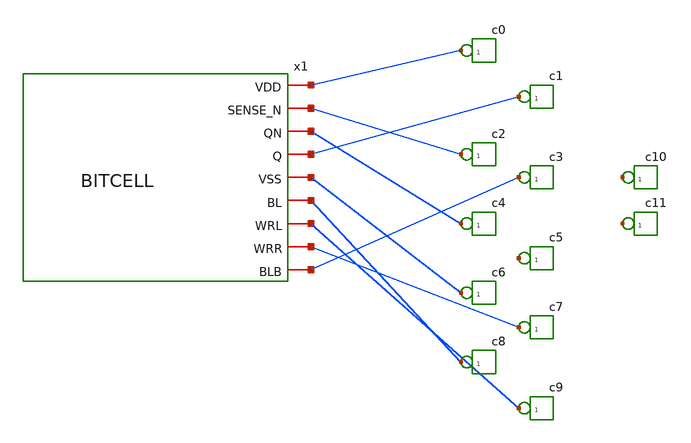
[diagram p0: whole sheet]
** sch_path: top.sch
**.subckt top
x1 net1 net2 net3 net4 net5 net6 net7 net8 net9 BITCELL
*connector(1,1) ?1 net1
*connector(1,1) ?1 net4
*connector(1,1) ?1 net2
*connector(1,1) ?1 net9
*connector(1,1) ?1 net3
*connector(1,1) ?1 net10
*connector(1,1) ?1 net5
*connector(1,1) ?1 net8
*connector(1,1) ?1 net6
*connector(1,1) ?1 net7
*connector(1,1) ?1 net11
*connector(1,1) ?1 net12
**.ends

* expanding   symbol:  /home/jackclar/mramSkywater/BITCELL.sym # of pins=9
** sym_path: BITCELL.sym
** sch_path: BITCELL.sch
.subckt BITCELL VDD SENSE_N QN Q VSS BL WRL WRR BLB
*.iopin VDD
*.iopin SENSE_N
*.iopin QN
*.iopin Q
*.iopin VSS
*.iopin BL
*.iopin WRR
*.iopin WRL
*.iopin BLB
x1 VDD SENSE_N QN Q VSS net2 net1 SENSEAMP
XR1 net1 BLB sky130_fd_pr__PMAMTJ Diameter=80E-9 t_fre=1.8E-9 t_ox=1.1E-9 T0=300 JOULE=2 IS=1
+ TMR_G=1.1 IC_G=1 RA_G=1
XR2 net2 BLB sky130_fd_pr__PMAMTJ Diameter=80E-9 t_fre=1.8E-9 t_ox=1.1E-9 T0=300 JOULE=2 IS=1
+ TMR_G=1.1 IC_G=1 RA_G=1
XM1 net1 WRL BL VSS sky130_fd_pr__nfet_01v8 L=0.15 W=1 nf=1 ad='int((nf+1)/2) * W/nf * 0.29' as='int((nf+2)/2) * W/nf * 0.29'
+ pd='2*int((nf+1)/2) * (W/nf + 0.29)' ps='2*int((nf+2)/2) * (W/nf + 0.29)' nrd='0.29 / W' nrs='0.29 / W'
+ sa=0 sb=0 sd=0 mult=1 m=1
XM2 net2 WRR BL VSS sky130_fd_pr__nfet_01v8 L=0.15 W=1 nf=1 ad='int((nf+1)/2) * W/nf * 0.29' as='int((nf+2)/2) * W/nf * 0.29'
+ pd='2*int((nf+1)/2) * (W/nf + 0.29)' ps='2*int((nf+2)/2) * (W/nf + 0.29)' nrd='0.29 / W' nrs='0.29 / W'
+ sa=0 sb=0 sd=0 mult=1 m=1
.ends


* expanding   symbol:  /home/jackclar/mramSkywater/SENSEAMP.sym # of pins=7
** sym_path: SENSEAMP.sym
** sch_path: SENSEAMP.sch
.subckt SENSEAMP VDD SENSE_N QN Q VSS I0 I1
*.iopin I1
*.iopin I0
*.iopin Q
*.iopin QN
*.iopin SENSE_N
*.iopin VDD
*.iopin VSS
XM3 Q SENSE_N VDD VDD sky130_fd_pr__pfet_01v8 L=0.15 W=1 nf=1 ad='int((nf+1)/2) * W/nf * 0.29' as='int((nf+2)/2) * W/nf * 0.29'
+ pd='2*int((nf+1)/2) * (W/nf + 0.29)' ps='2*int((nf+2)/2) * (W/nf + 0.29)' nrd='0.29 / W' nrs='0.29 / W'
+ sa=0 sb=0 sd=0 mult=1 m=1
XM1 Q QN VDD VDD sky130_fd_pr__pfet_01v8 L=0.15 W=1 nf=1 ad='int((nf+1)/2) * W/nf * 0.29' as='int((nf+2)/2) * W/nf * 0.29'
+ pd='2*int((nf+1)/2) * (W/nf + 0.29)' ps='2*int((nf+2)/2) * (W/nf + 0.29)' nrd='0.29 / W' nrs='0.29 / W'
+ sa=0 sb=0 sd=0 mult=1 m=1
XM2 QN Q VDD VDD sky130_fd_pr__pfet_01v8 L=0.15 W=1 nf=1 ad='int((nf+1)/2) * W/nf * 0.29' as='int((nf+2)/2) * W/nf * 0.29'
+ pd='2*int((nf+1)/2) * (W/nf + 0.29)' ps='2*int((nf+2)/2) * (W/nf + 0.29)' nrd='0.29 / W' nrs='0.29 / W'
+ sa=0 sb=0 sd=0 mult=1 m=1
XM4 QN SENSE_N VDD net3 sky130_fd_pr__pfet_01v8 L=0.15 W=1 nf=1 ad='int((nf+1)/2) * W/nf * 0.29' as='int((nf+2)/2) * W/nf * 0.29'
+ pd='2*int((nf+1)/2) * (W/nf + 0.29)' ps='2*int((nf+2)/2) * (W/nf + 0.29)' nrd='0.29 / W' nrs='0.29 / W'
+ sa=0 sb=0 sd=0 mult=1 m=1
XM5 QN Q net2 VSS sky130_fd_pr__nfet_01v8 L=0.15 W=1 nf=1 ad='int((nf+1)/2) * W/nf * 0.29' as='int((nf+2)/2) * W/nf * 0.29'
+ pd='2*int((nf+1)/2) * (W/nf + 0.29)' ps='2*int((nf+2)/2) * (W/nf + 0.29)' nrd='0.29 / W' nrs='0.29 / W'
+ sa=0 sb=0 sd=0 mult=1 m=1
XM6 Q QN net1 VSS sky130_fd_pr__nfet_01v8 L=0.15 W=1 nf=1 ad='int((nf+1)/2) * W/nf * 0.29' as='int((nf+2)/2) * W/nf * 0.29'
+ pd='2*int((nf+1)/2) * (W/nf + 0.29)' ps='2*int((nf+2)/2) * (W/nf + 0.29)' nrd='0.29 / W' nrs='0.29 / W'
+ sa=0 sb=0 sd=0 mult=1 m=1
**** begin user architecture code
I1
**** end user architecture code
.ends

.end
